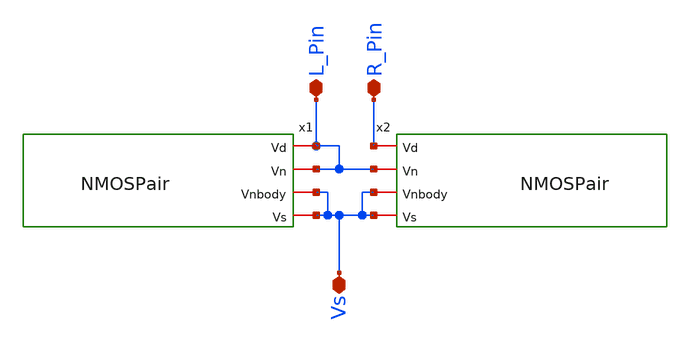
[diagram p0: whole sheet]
** sch_path: xschem/PrimalStructures/Level2/ConnectedNMOSPair.sch
**.subckt ConnectedNMOSPair L_Pin R_Pin Vs
*.iopin L_Pin
*.iopin R_Pin
*.iopin Vs
x1 L_Pin L_Pin Vs Vs NMOSPair
x2 R_Pin L_Pin Vs Vs NMOSPair
**.ends
.end
